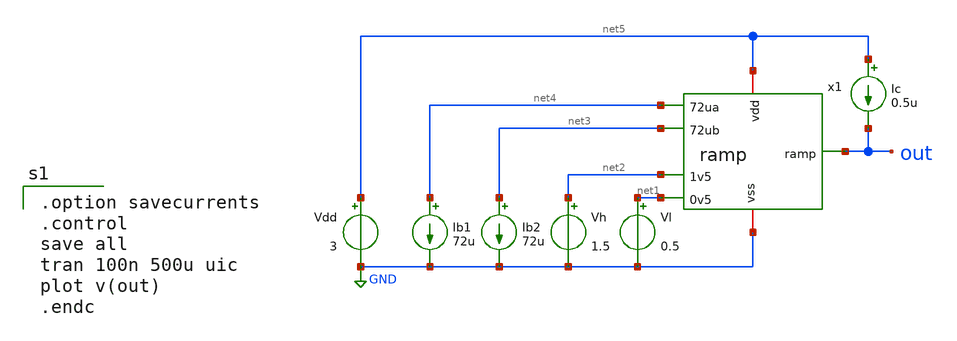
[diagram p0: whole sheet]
** sch_path: member_project/DCDC/ShuntaroOHNO/xschem/ramp_tran.sch
**.subckt ramp_tran
Vdd net5 GND 3
x1 net5 out net4 net2 net3 net1 GND ramp
Vl net1 GND 0.5
Vh net2 GND 1.5
Ic net5 out 0.5u
Ib1 net4 GND 72u
Ib2 net3 GND 72u
**** begin user architecture code
 .include $::LIB/ip62_models

.option savecurrents
.control
save all
tran 100n 500u uic
plot v(out)
.endc

**** end user architecture code
**.ends
.GLOBAL GND
.end
